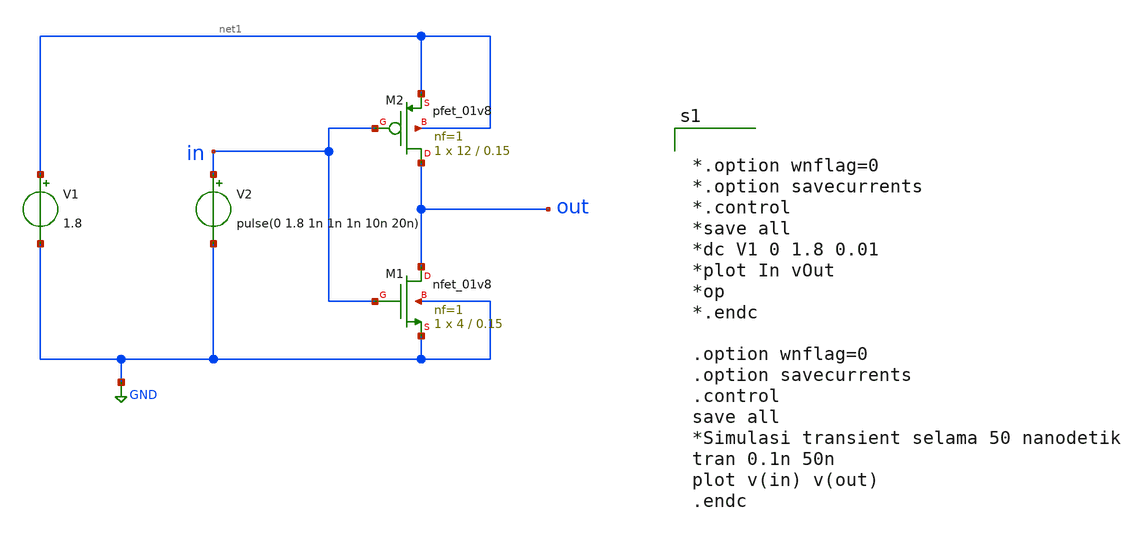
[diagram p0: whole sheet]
** sch_path: direktori/skematik/inverter.sch
**.subckt inverter
XM1 out in GND GND sky130_fd_pr__nfet_01v8 L=0.15 W=4 nf=1 ad='int((1 + 1)/2) * 4 / 1 * 0.29' as='int((1 + 2)/2) * 4 / 1 * 0.29'
+ pd='2*int((1 + 1)/2) * (4 / 1 + 0.29)' ps='2*int((1 + 2)/2) * (4 / 1 + 0.29)' nrd='0.29 / 4 ' nrs='0.29 / 4 '
+ sa=0 sb=0 sd=0 mult=1 m=1
XM2 out in net1 net1 sky130_fd_pr__pfet_01v8 L=0.15 W=12 nf=1 ad='int((1 + 1)/2) * 12 / 1 * 0.29' as='int((1 + 2)/2) * 12 / 1 * 0.29'
+ pd='2*int((1 + 1)/2) * (12 / 1 + 0.29)' ps='2*int((1 + 2)/2) * (12 / 1 + 0.29)' nrd='0.29 / 12 ' nrs='0.29 / 12 '
+ sa=0 sb=0 sd=0 mult=1 m=1
V1 net1 GND 1.8
V2 in GND pulse(0 1.8 1n 1n 1n 10n 20n)
**** begin user architecture code
 .lib /foss/pdks/ciel/sky130/versions/7b70722e33c03fcb5dabcf4d479fb0822d9251c9/sky130A/libs.tech/ngspice/sky130.lib.spice tt

.param mc_mm_switch=0
.param mc_pr_switch=1



*.option wnflag=0
*.option savecurrents
*.control
*save all
*dc V1 0 1.8 0.01
*plot In vOut
*op
*.endc

.option wnflag=0
.option savecurrents
.control
save all
*Simulasi transient selama 50 nanodetik
tran 0.1n 50n
plot v(in) v(out)
.endc


**** end user architecture code
**.ends
.GLOBAL GND
.end
